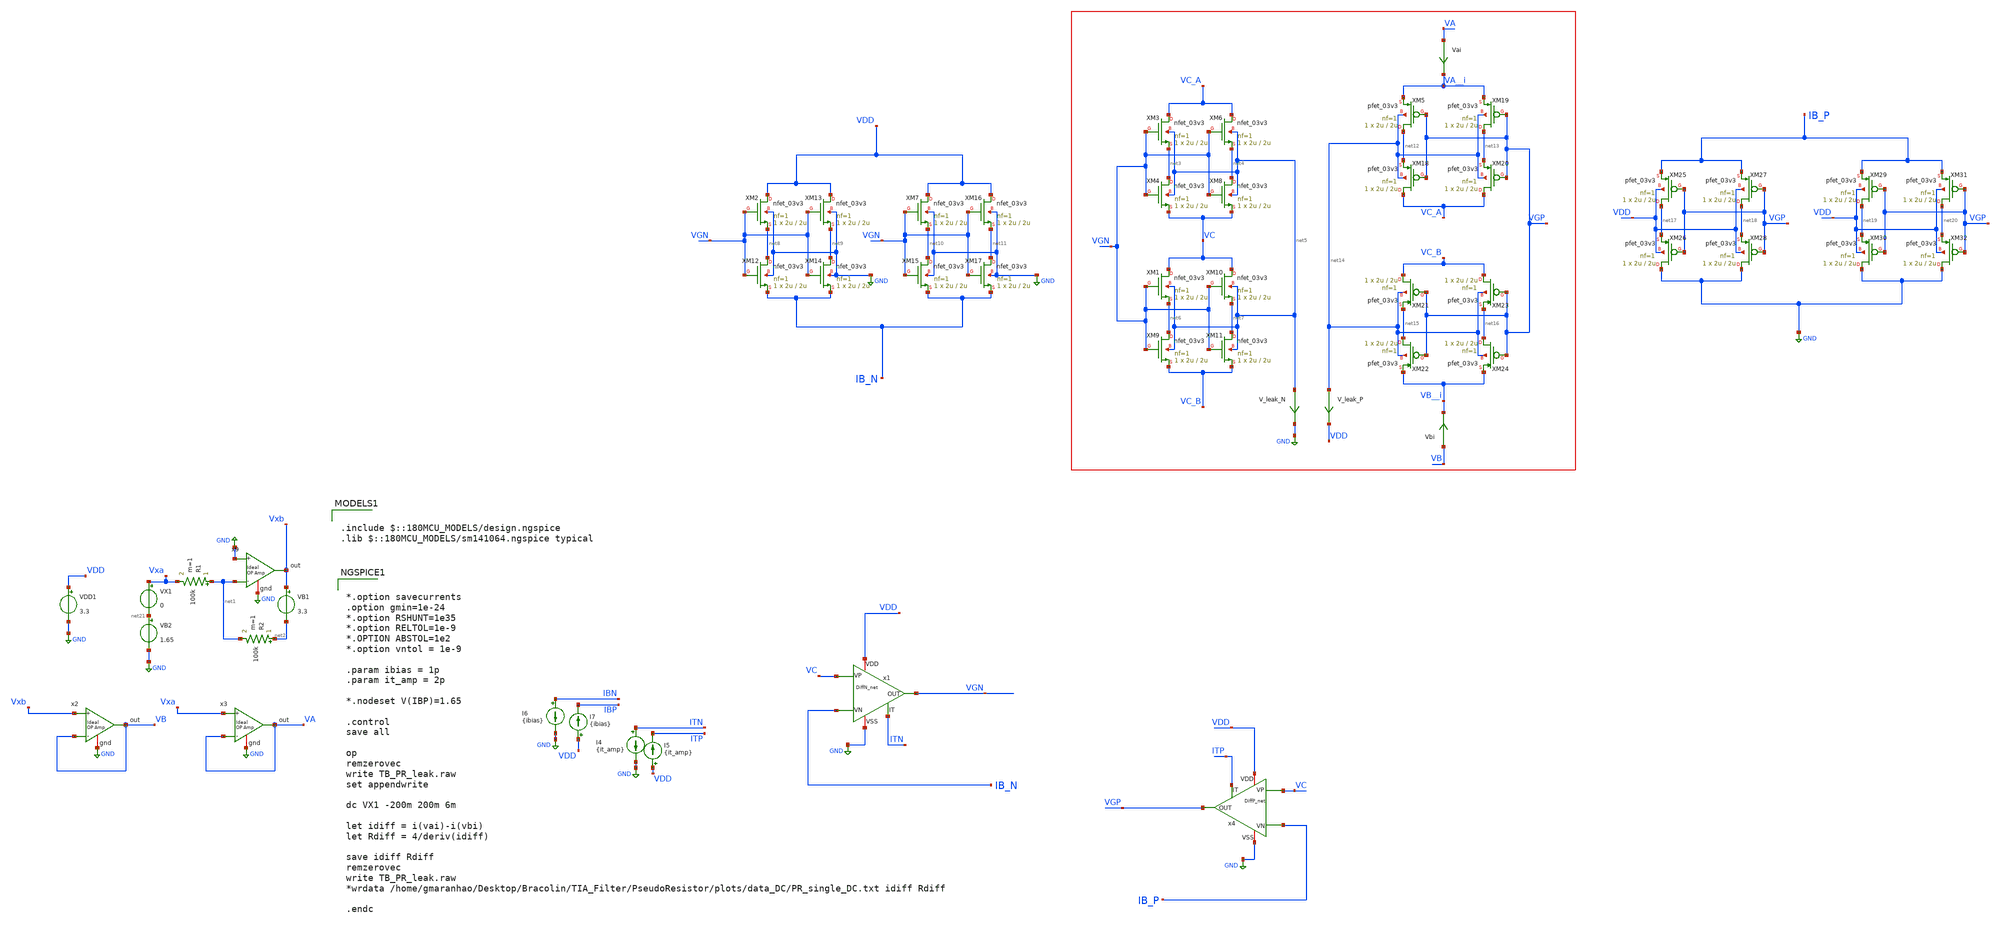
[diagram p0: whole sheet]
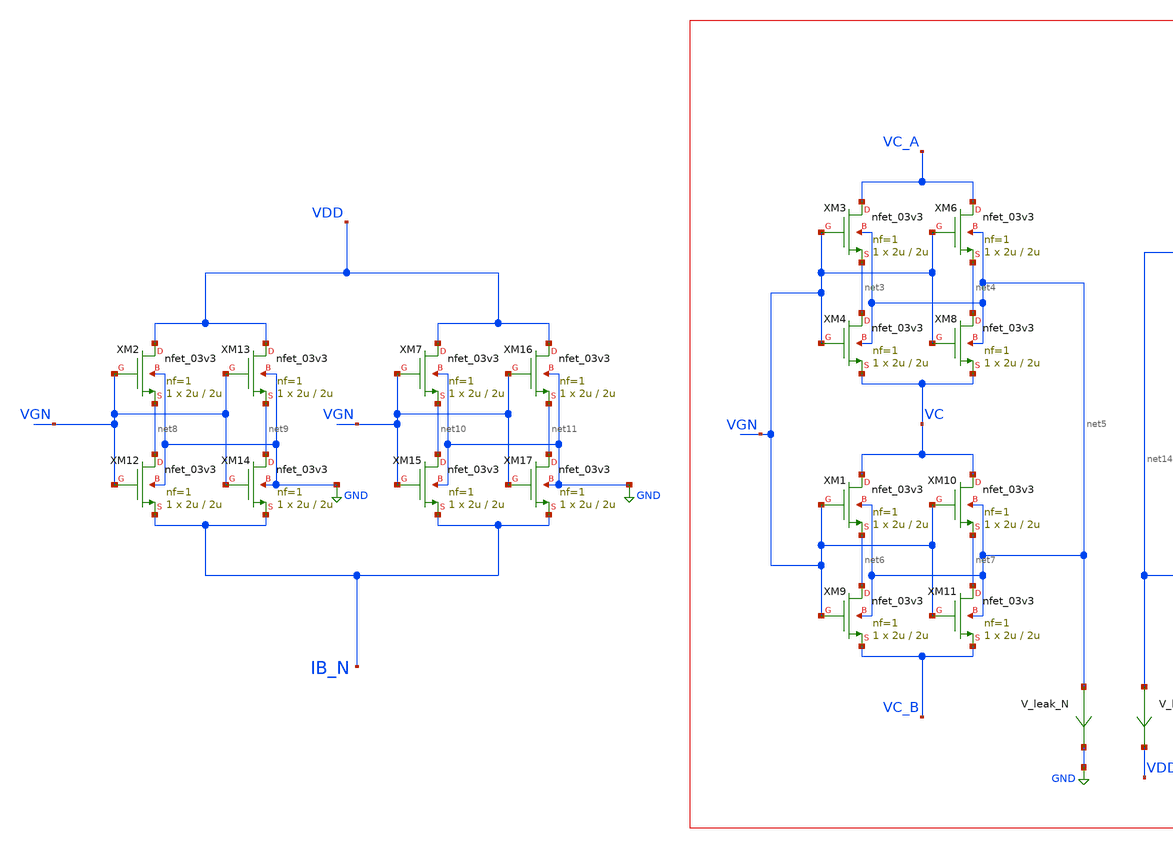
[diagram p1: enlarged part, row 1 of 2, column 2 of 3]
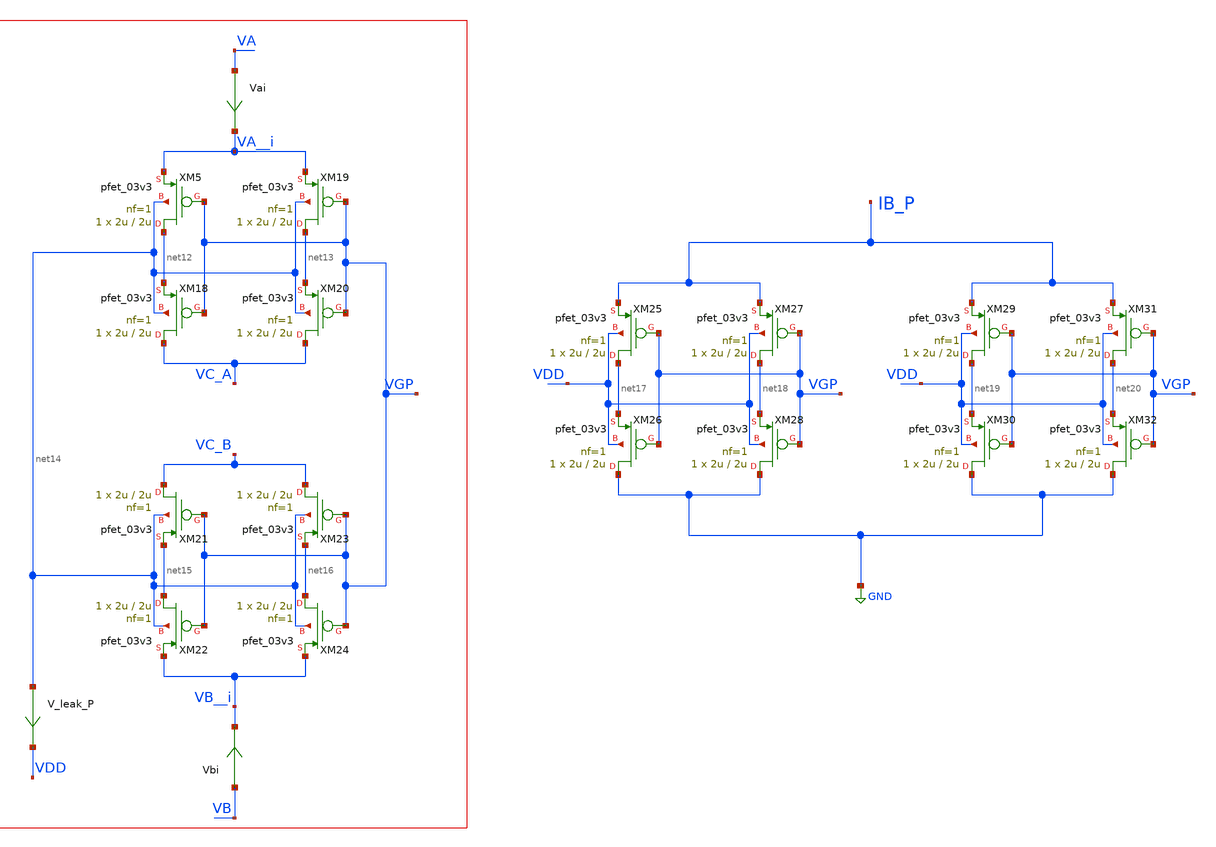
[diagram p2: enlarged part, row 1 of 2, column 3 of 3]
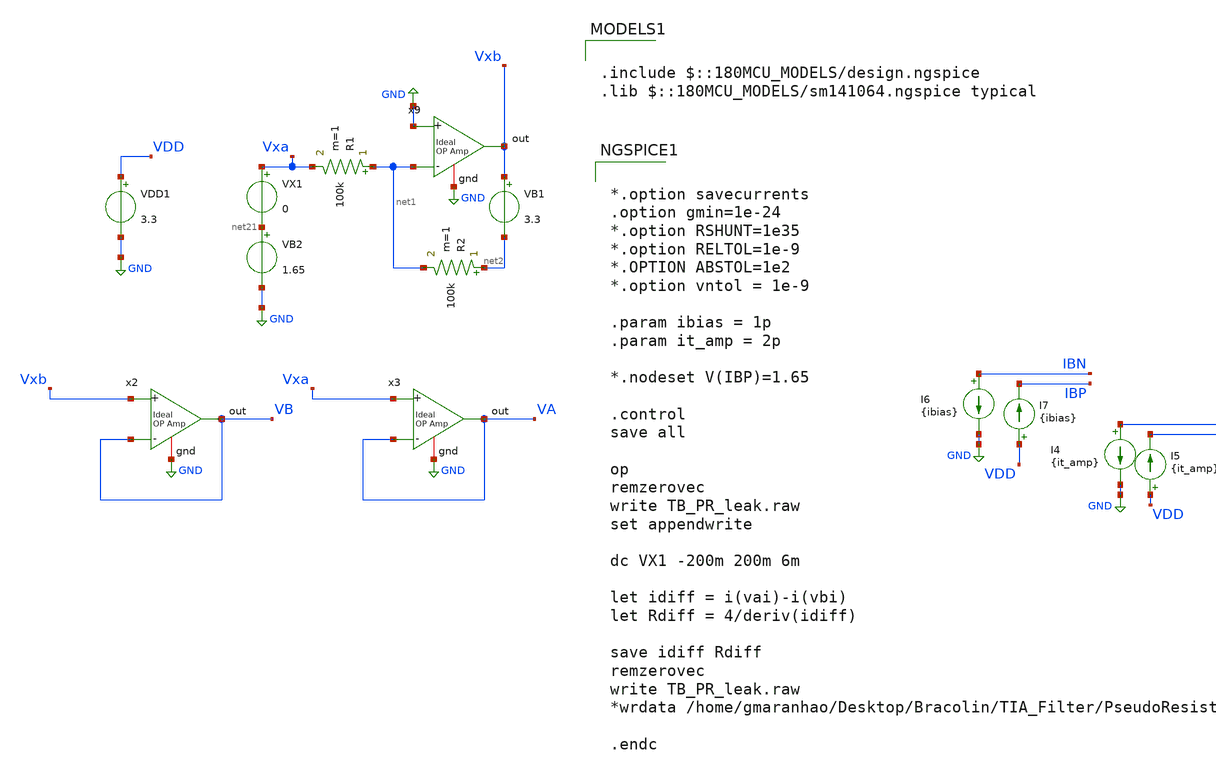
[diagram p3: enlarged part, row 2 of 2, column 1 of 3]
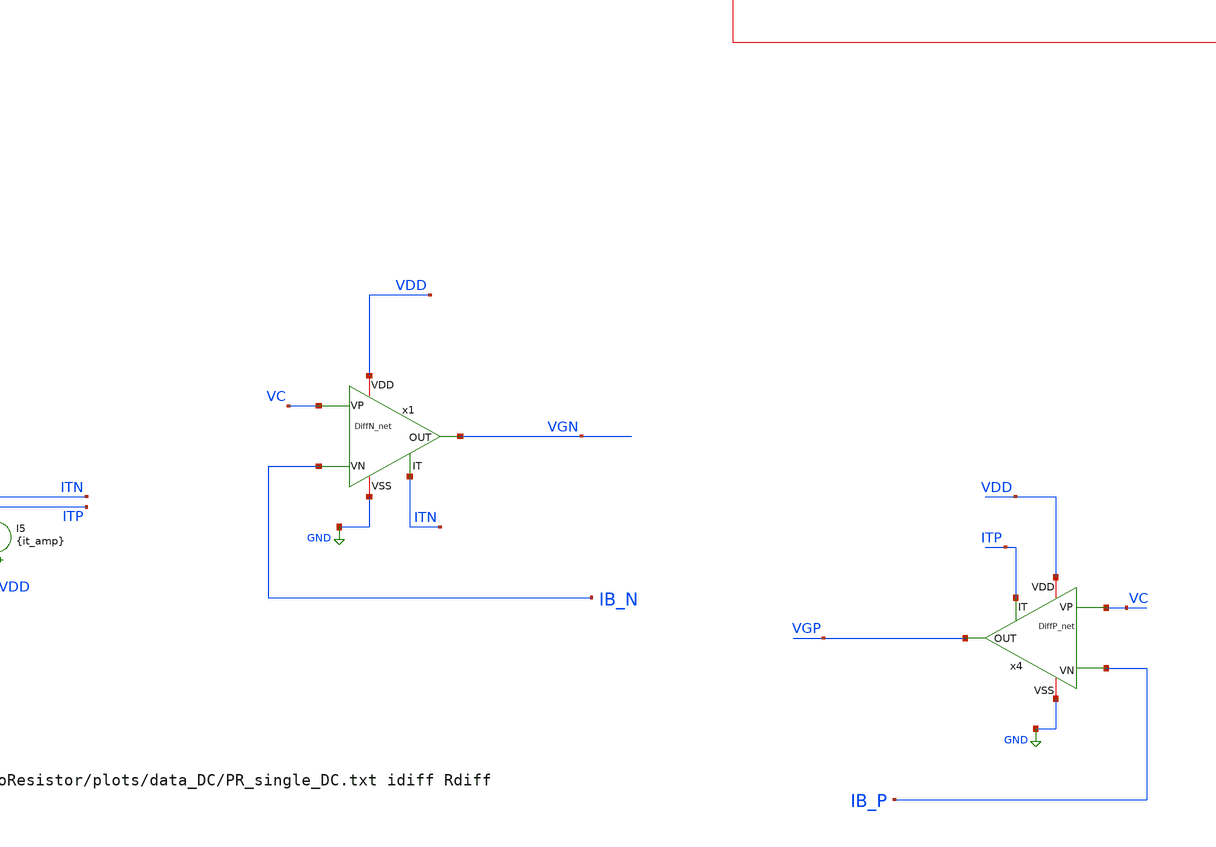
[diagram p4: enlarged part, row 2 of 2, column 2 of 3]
** sch_path: TIA_Filter/PseudoResistor/TB_PR_leak.sch
**.subckt TB_PR_leak
VDD1 VDD GND 3.3
VX1 Vxa net21 0
VB1 Vxb net2 3.3
R1 net1 Vxa 100k m=1
R2 net2 net1 100k m=1
VB2 net21 GND 1.65
x2 VB Vxb VB GND ampOp_ideal
x3 VA Vxa VA GND ampOp_ideal
x9 Vxb GND net1 GND ampOp_ideal
XM3 VC_A VGN net3 net5 nfet_03v3 L=2u W=2u nf=1 ad='int((nf+1)/2) * W/nf * 0.18u' as='int((nf+2)/2) * W/nf * 0.18u'
+ pd='2*int((nf+1)/2) * (W/nf + 0.18u)' ps='2*int((nf+2)/2) * (W/nf + 0.18u)' nrd='0.18u / W' nrs='0.18u / W'
+ sa=0 sb=0 sd=0 m=1
XM4 net3 VGN VC net5 nfet_03v3 L=2u W=2u nf=1 ad='int((nf+1)/2) * W/nf * 0.18u' as='int((nf+2)/2) * W/nf * 0.18u'
+ pd='2*int((nf+1)/2) * (W/nf + 0.18u)' ps='2*int((nf+2)/2) * (W/nf + 0.18u)' nrd='0.18u / W' nrs='0.18u / W'
+ sa=0 sb=0 sd=0 m=1
XM6 VC_A VGN net4 net5 nfet_03v3 L=2u W=2u nf=1 ad='int((nf+1)/2) * W/nf * 0.18u' as='int((nf+2)/2) * W/nf * 0.18u'
+ pd='2*int((nf+1)/2) * (W/nf + 0.18u)' ps='2*int((nf+2)/2) * (W/nf + 0.18u)' nrd='0.18u / W' nrs='0.18u / W'
+ sa=0 sb=0 sd=0 m=1
XM8 net4 VGN VC net5 nfet_03v3 L=2u W=2u nf=1 ad='int((nf+1)/2) * W/nf * 0.18u' as='int((nf+2)/2) * W/nf * 0.18u'
+ pd='2*int((nf+1)/2) * (W/nf + 0.18u)' ps='2*int((nf+2)/2) * (W/nf + 0.18u)' nrd='0.18u / W' nrs='0.18u / W'
+ sa=0 sb=0 sd=0 m=1
XM1 VC VGN net6 net5 nfet_03v3 L=2u W=2u nf=1 ad='int((nf+1)/2) * W/nf * 0.18u' as='int((nf+2)/2) * W/nf * 0.18u'
+ pd='2*int((nf+1)/2) * (W/nf + 0.18u)' ps='2*int((nf+2)/2) * (W/nf + 0.18u)' nrd='0.18u / W' nrs='0.18u / W'
+ sa=0 sb=0 sd=0 m=1
XM9 net6 VGN VC_B net5 nfet_03v3 L=2u W=2u nf=1 ad='int((nf+1)/2) * W/nf * 0.18u' as='int((nf+2)/2) * W/nf * 0.18u'
+ pd='2*int((nf+1)/2) * (W/nf + 0.18u)' ps='2*int((nf+2)/2) * (W/nf + 0.18u)' nrd='0.18u / W' nrs='0.18u / W'
+ sa=0 sb=0 sd=0 m=1
XM10 VC VGN net7 net5 nfet_03v3 L=2u W=2u nf=1 ad='int((nf+1)/2) * W/nf * 0.18u' as='int((nf+2)/2) * W/nf * 0.18u'
+ pd='2*int((nf+1)/2) * (W/nf + 0.18u)' ps='2*int((nf+2)/2) * (W/nf + 0.18u)' nrd='0.18u / W' nrs='0.18u / W'
+ sa=0 sb=0 sd=0 m=1
XM11 net7 VGN VC_B net5 nfet_03v3 L=2u W=2u nf=1 ad='int((nf+1)/2) * W/nf * 0.18u' as='int((nf+2)/2) * W/nf * 0.18u'
+ pd='2*int((nf+1)/2) * (W/nf + 0.18u)' ps='2*int((nf+2)/2) * (W/nf + 0.18u)' nrd='0.18u / W' nrs='0.18u / W'
+ sa=0 sb=0 sd=0 m=1
XM2 VDD VGN net8 GND nfet_03v3 L=2u W=2u nf=1 ad='int((nf+1)/2) * W/nf * 0.18u' as='int((nf+2)/2) * W/nf * 0.18u'
+ pd='2*int((nf+1)/2) * (W/nf + 0.18u)' ps='2*int((nf+2)/2) * (W/nf + 0.18u)' nrd='0.18u / W' nrs='0.18u / W'
+ sa=0 sb=0 sd=0 m=1
XM12 net8 VGN IB_N GND nfet_03v3 L=2u W=2u nf=1 ad='int((nf+1)/2) * W/nf * 0.18u' as='int((nf+2)/2) * W/nf * 0.18u'
+ pd='2*int((nf+1)/2) * (W/nf + 0.18u)' ps='2*int((nf+2)/2) * (W/nf + 0.18u)' nrd='0.18u / W' nrs='0.18u / W'
+ sa=0 sb=0 sd=0 m=1
XM13 VDD VGN net9 GND nfet_03v3 L=2u W=2u nf=1 ad='int((nf+1)/2) * W/nf * 0.18u' as='int((nf+2)/2) * W/nf * 0.18u'
+ pd='2*int((nf+1)/2) * (W/nf + 0.18u)' ps='2*int((nf+2)/2) * (W/nf + 0.18u)' nrd='0.18u / W' nrs='0.18u / W'
+ sa=0 sb=0 sd=0 m=1
XM14 net9 VGN IB_N GND nfet_03v3 L=2u W=2u nf=1 ad='int((nf+1)/2) * W/nf * 0.18u' as='int((nf+2)/2) * W/nf * 0.18u'
+ pd='2*int((nf+1)/2) * (W/nf + 0.18u)' ps='2*int((nf+2)/2) * (W/nf + 0.18u)' nrd='0.18u / W' nrs='0.18u / W'
+ sa=0 sb=0 sd=0 m=1
XM7 VDD VGN net10 GND nfet_03v3 L=2u W=2u nf=1 ad='int((nf+1)/2) * W/nf * 0.18u' as='int((nf+2)/2) * W/nf * 0.18u'
+ pd='2*int((nf+1)/2) * (W/nf + 0.18u)' ps='2*int((nf+2)/2) * (W/nf + 0.18u)' nrd='0.18u / W' nrs='0.18u / W'
+ sa=0 sb=0 sd=0 m=1
XM15 net10 VGN IB_N GND nfet_03v3 L=2u W=2u nf=1 ad='int((nf+1)/2) * W/nf * 0.18u' as='int((nf+2)/2) * W/nf * 0.18u'
+ pd='2*int((nf+1)/2) * (W/nf + 0.18u)' ps='2*int((nf+2)/2) * (W/nf + 0.18u)' nrd='0.18u / W' nrs='0.18u / W'
+ sa=0 sb=0 sd=0 m=1
XM16 VDD VGN net11 GND nfet_03v3 L=2u W=2u nf=1 ad='int((nf+1)/2) * W/nf * 0.18u' as='int((nf+2)/2) * W/nf * 0.18u'
+ pd='2*int((nf+1)/2) * (W/nf + 0.18u)' ps='2*int((nf+2)/2) * (W/nf + 0.18u)' nrd='0.18u / W' nrs='0.18u / W'
+ sa=0 sb=0 sd=0 m=1
XM17 net11 VGN IB_N GND nfet_03v3 L=2u W=2u nf=1 ad='int((nf+1)/2) * W/nf * 0.18u' as='int((nf+2)/2) * W/nf * 0.18u'
+ pd='2*int((nf+1)/2) * (W/nf + 0.18u)' ps='2*int((nf+2)/2) * (W/nf + 0.18u)' nrd='0.18u / W' nrs='0.18u / W'
+ sa=0 sb=0 sd=0 m=1
XM5 net12 VGP VA__i net14 pfet_03v3 L=2u W=2u nf=1 ad='int((nf+1)/2) * W/nf * 0.18u' as='int((nf+2)/2) * W/nf * 0.18u'
+ pd='2*int((nf+1)/2) * (W/nf + 0.18u)' ps='2*int((nf+2)/2) * (W/nf + 0.18u)' nrd='0.18u / W' nrs='0.18u / W'
+ sa=0 sb=0 sd=0 m=1
XM18 VC_A VGP net12 net14 pfet_03v3 L=2u W=2u nf=1 ad='int((nf+1)/2) * W/nf * 0.18u' as='int((nf+2)/2) * W/nf * 0.18u'
+ pd='2*int((nf+1)/2) * (W/nf + 0.18u)' ps='2*int((nf+2)/2) * (W/nf + 0.18u)' nrd='0.18u / W' nrs='0.18u / W'
+ sa=0 sb=0 sd=0 m=1
XM19 net13 VGP VA__i net14 pfet_03v3 L=2u W=2u nf=1 ad='int((nf+1)/2) * W/nf * 0.18u' as='int((nf+2)/2) * W/nf * 0.18u'
+ pd='2*int((nf+1)/2) * (W/nf + 0.18u)' ps='2*int((nf+2)/2) * (W/nf + 0.18u)' nrd='0.18u / W' nrs='0.18u / W'
+ sa=0 sb=0 sd=0 m=1
XM20 VC_A VGP net13 net14 pfet_03v3 L=2u W=2u nf=1 ad='int((nf+1)/2) * W/nf * 0.18u' as='int((nf+2)/2) * W/nf * 0.18u'
+ pd='2*int((nf+1)/2) * (W/nf + 0.18u)' ps='2*int((nf+2)/2) * (W/nf + 0.18u)' nrd='0.18u / W' nrs='0.18u / W'
+ sa=0 sb=0 sd=0 m=1
XM21 VC_B VGP net15 net14 pfet_03v3 L=2u W=2u nf=1 ad='int((nf+1)/2) * W/nf * 0.18u' as='int((nf+2)/2) * W/nf * 0.18u'
+ pd='2*int((nf+1)/2) * (W/nf + 0.18u)' ps='2*int((nf+2)/2) * (W/nf + 0.18u)' nrd='0.18u / W' nrs='0.18u / W'
+ sa=0 sb=0 sd=0 m=1
XM22 net15 VGP VB__i net14 pfet_03v3 L=2u W=2u nf=1 ad='int((nf+1)/2) * W/nf * 0.18u' as='int((nf+2)/2) * W/nf * 0.18u'
+ pd='2*int((nf+1)/2) * (W/nf + 0.18u)' ps='2*int((nf+2)/2) * (W/nf + 0.18u)' nrd='0.18u / W' nrs='0.18u / W'
+ sa=0 sb=0 sd=0 m=1
XM23 VC_B VGP net16 net14 pfet_03v3 L=2u W=2u nf=1 ad='int((nf+1)/2) * W/nf * 0.18u' as='int((nf+2)/2) * W/nf * 0.18u'
+ pd='2*int((nf+1)/2) * (W/nf + 0.18u)' ps='2*int((nf+2)/2) * (W/nf + 0.18u)' nrd='0.18u / W' nrs='0.18u / W'
+ sa=0 sb=0 sd=0 m=1
XM24 net16 VGP VB__i net14 pfet_03v3 L=2u W=2u nf=1 ad='int((nf+1)/2) * W/nf * 0.18u' as='int((nf+2)/2) * W/nf * 0.18u'
+ pd='2*int((nf+1)/2) * (W/nf + 0.18u)' ps='2*int((nf+2)/2) * (W/nf + 0.18u)' nrd='0.18u / W' nrs='0.18u / W'
+ sa=0 sb=0 sd=0 m=1
XM25 net17 VGP IB_P VDD pfet_03v3 L=2u W=2u nf=1 ad='int((nf+1)/2) * W/nf * 0.18u' as='int((nf+2)/2) * W/nf * 0.18u'
+ pd='2*int((nf+1)/2) * (W/nf + 0.18u)' ps='2*int((nf+2)/2) * (W/nf + 0.18u)' nrd='0.18u / W' nrs='0.18u / W'
+ sa=0 sb=0 sd=0 m=1
XM26 GND VGP net17 VDD pfet_03v3 L=2u W=2u nf=1 ad='int((nf+1)/2) * W/nf * 0.18u' as='int((nf+2)/2) * W/nf * 0.18u'
+ pd='2*int((nf+1)/2) * (W/nf + 0.18u)' ps='2*int((nf+2)/2) * (W/nf + 0.18u)' nrd='0.18u / W' nrs='0.18u / W'
+ sa=0 sb=0 sd=0 m=1
XM27 net18 VGP IB_P VDD pfet_03v3 L=2u W=2u nf=1 ad='int((nf+1)/2) * W/nf * 0.18u' as='int((nf+2)/2) * W/nf * 0.18u'
+ pd='2*int((nf+1)/2) * (W/nf + 0.18u)' ps='2*int((nf+2)/2) * (W/nf + 0.18u)' nrd='0.18u / W' nrs='0.18u / W'
+ sa=0 sb=0 sd=0 m=1
XM28 GND VGP net18 VDD pfet_03v3 L=2u W=2u nf=1 ad='int((nf+1)/2) * W/nf * 0.18u' as='int((nf+2)/2) * W/nf * 0.18u'
+ pd='2*int((nf+1)/2) * (W/nf + 0.18u)' ps='2*int((nf+2)/2) * (W/nf + 0.18u)' nrd='0.18u / W' nrs='0.18u / W'
+ sa=0 sb=0 sd=0 m=1
XM29 net19 VGP IB_P VDD pfet_03v3 L=2u W=2u nf=1 ad='int((nf+1)/2) * W/nf * 0.18u' as='int((nf+2)/2) * W/nf * 0.18u'
+ pd='2*int((nf+1)/2) * (W/nf + 0.18u)' ps='2*int((nf+2)/2) * (W/nf + 0.18u)' nrd='0.18u / W' nrs='0.18u / W'
+ sa=0 sb=0 sd=0 m=1
XM30 GND VGP net19 VDD pfet_03v3 L=2u W=2u nf=1 ad='int((nf+1)/2) * W/nf * 0.18u' as='int((nf+2)/2) * W/nf * 0.18u'
+ pd='2*int((nf+1)/2) * (W/nf + 0.18u)' ps='2*int((nf+2)/2) * (W/nf + 0.18u)' nrd='0.18u / W' nrs='0.18u / W'
+ sa=0 sb=0 sd=0 m=1
XM31 net20 VGP IB_P VDD pfet_03v3 L=2u W=2u nf=1 ad='int((nf+1)/2) * W/nf * 0.18u' as='int((nf+2)/2) * W/nf * 0.18u'
+ pd='2*int((nf+1)/2) * (W/nf + 0.18u)' ps='2*int((nf+2)/2) * (W/nf + 0.18u)' nrd='0.18u / W' nrs='0.18u / W'
+ sa=0 sb=0 sd=0 m=1
XM32 GND VGP net20 VDD pfet_03v3 L=2u W=2u nf=1 ad='int((nf+1)/2) * W/nf * 0.18u' as='int((nf+2)/2) * W/nf * 0.18u'
+ pd='2*int((nf+1)/2) * (W/nf + 0.18u)' ps='2*int((nf+2)/2) * (W/nf + 0.18u)' nrd='0.18u / W' nrs='0.18u / W'
+ sa=0 sb=0 sd=0 m=1
x1 IB_N VC VGN ITN VDD GND DiffN_net
x4 IB_P VC VGP ITP VDD GND DiffP_net
I4 ITN GND {it_amp}
I5 VDD ITP {it_amp}
I6 IBN GND {ibias}
I7 VDD IBP {ibias}
V_leak_N net5 GND 0
.save i(v_leak_n)
V_leak_P net14 VDD 0
.save i(v_leak_p)
Vbi VB VB__i 0
.save i(vbi)
Vai VA VA__i 0
.save i(vai)
**** begin user architecture code

.include $::180MCU_MODELS/design.ngspice
.lib $::180MCU_MODELS/sm141064.ngspice typical




*.option savecurrents
.option gmin=1e-24
*.option RSHUNT=1e35
*.option RELTOL=1e-9
*.OPTION ABSTOL=1e2
*.option vntol = 1e-9

.param ibias = 1p
.param it_amp = 2p

*.nodeset V(IBP)=1.65

.control
save all

op
remzerovec
write TB_PR_leak.raw
set appendwrite

dc VX1 -200m 200m 6m

let idiff = i(vai)-i(vbi)
let Rdiff = 4/deriv(idiff)

save idiff Rdiff
remzerovec
write TB_PR_leak.raw
*wrdata /home/gmaranhao/Desktop/Bracolin/TIA_Filter/PseudoResistor/plots/data_DC/PR_single_DC.txt
*+ idiff Rdiff

.endc


**** end user architecture code
**.ends
.GLOBAL GND
.end
